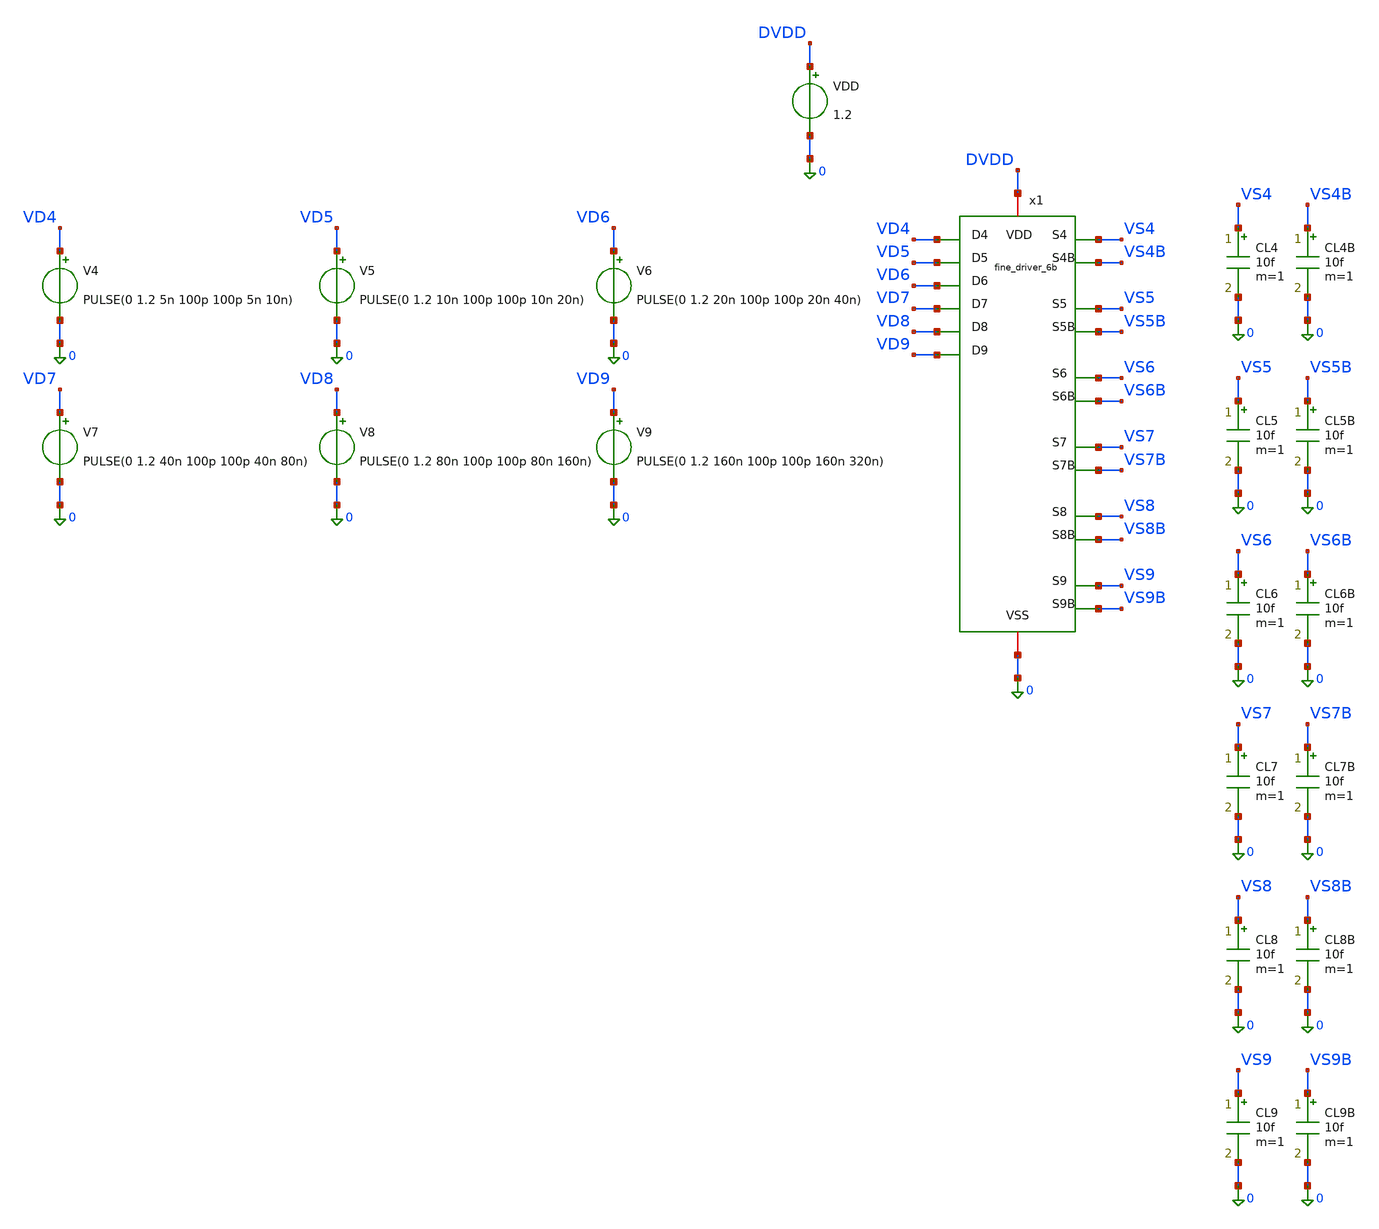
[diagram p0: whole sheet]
** sch_path: designs/libs/core_digital/fine_driver_6b/tb_fine_driver_6b.sch
**.subckt tb_fine_driver_6b
x1 VD4 VD7 VS4 VS4B DVDD 0 VD5 VD6 VD8 VD9 VS5 VS5B VS6 VS6B VS7 VS7B VS8 VS8B VS9 VS9B
+ fine_driver_6b
VDD DVDD 0 1.2
V6 VD6 0 PULSE(0 1.2 20n 100p 100p 20n 40n)
V5 VD5 0 PULSE(0 1.2 10n 100p 100p 10n 20n)
V4 VD4 0 PULSE(0 1.2 5n 100p 100p 5n 10n)
V7 VD7 0 PULSE(0 1.2 40n 100p 100p 40n 80n)
V8 VD8 0 PULSE(0 1.2 80n 100p 100p 80n 160n)
V9 VD9 0 PULSE(0 1.2 160n 100p 100p 160n 320n)
CL4 VS4 0 10f m=1
CL4B VS4B 0 10f m=1
CL5 VS5 0 10f m=1
CL5B VS5B 0 10f m=1
CL6 VS6 0 10f m=1
CL6B VS6B 0 10f m=1
CL7 VS7 0 10f m=1
CL7B VS7B 0 10f m=1
CL8 VS8 0 10f m=1
CL8B VS8B 0 10f m=1
CL9 VS9 0 10f m=1
CL9B VS9B 0 10f m=1
**** begin user architecture code

.lib cornerMOSlv.lib mos_tt
.include /foss/pdks/ihp-sg13cmos5l/libs.ref/sg13cmos5l_stdcell/spice/sg13cmos5l_stdcell.spice


.control
  tran 100p 320n
  write tb_fine_driver_6b.raw

  * Multi-trace offset plots for Lower 3 bits (D4, D5, D6)
  plot v(VD4) v(VS4)+1.5 v(VS4B)+3.0 title 'Bit 4: Input (VD4), True (VS4), Complement (VS4B)' xlabel
+ 'Time (s)' ylabel 'Voltage (V)'
  plot v(VD5) v(VS5)+1.5 v(VS5B)+3.0 title 'Bit 5: Input (VD5), True (VS5), Complement (VS5B)' xlabel
+ 'Time (s)' ylabel 'Voltage (V)'
  plot v(VD6) v(VS6)+1.5 v(VS6B)+3.0 title 'Bit 6: Input (VD6), True (VS6), Complement (VS6B)' xlabel
+ 'Time (s)' ylabel 'Voltage (V)'

  * Multi-trace offset plots for Upper 3 bits (D7, D8, D9)
  plot v(VD7) v(VS7)+1.5 v(VS7B)+3.0 title 'Bit 7: Input (VD7), True (VS7), Complement (VS7B)' xlabel
+ 'Time (s)' ylabel 'Voltage (V)'
  plot v(VD8) v(VS8)+1.5 v(VS8B)+3.0 title 'Bit 8: Input (VD8), True (VS8), Complement (VS8B)' xlabel
+ 'Time (s)' ylabel 'Voltage (V)'
  plot v(VD9) v(VS9)+1.5 v(VS9B)+3.0 title 'Bit 9: Input (VD9), True (VS9), Complement (VS9B)' xlabel
+ 'Time (s)' ylabel 'Voltage (V)'
.endc


**** end user architecture code
**.ends

* expanding   symbol:  fine_driver_6b.sym # of pins=20
** sym_path: fine_driver_6b.sym
** sch_path: fine_driver_6b.sch
.subckt fine_driver_6b D4 D7 S4 S4B VDD VSS D5 D6 D8 D9 S5 S5B S6 S6B S7 S7B S8 S8B S9 S9B
*.ipin D4
*.opin S4
*.opin S4B
*.iopin VDD
*.iopin VSS
*.ipin D5
*.opin S5
*.opin S5B
*.ipin D6
*.opin S6
*.opin S6B
*.ipin D7
*.opin S7
*.opin S7B
*.ipin D8
*.opin S8
*.opin S8B
*.ipin D9
*.opin S9
*.opin S9B
x1 S4 D4 VDD VSS sg13cmos5l_buf_1
x2 S4B D4 VDD VSS sg13cmos5l_inv_1
x3 S5 D5 VDD VSS sg13cmos5l_buf_1
x4 S5B D5 VDD VSS sg13cmos5l_inv_1
x5 S6 D6 VDD VSS sg13cmos5l_buf_1
x6 S6B D6 VDD VSS sg13cmos5l_inv_1
x7 S7 D7 VDD VSS sg13cmos5l_buf_1
x8 S7B D7 VDD VSS sg13cmos5l_inv_1
x9 S8 D8 VDD VSS sg13cmos5l_buf_1
x10 S8B D8 VDD VSS sg13cmos5l_inv_1
x11 S9 D9 VDD VSS sg13cmos5l_buf_1
x12 S9B D9 VDD VSS sg13cmos5l_inv_1
.ends

.end
